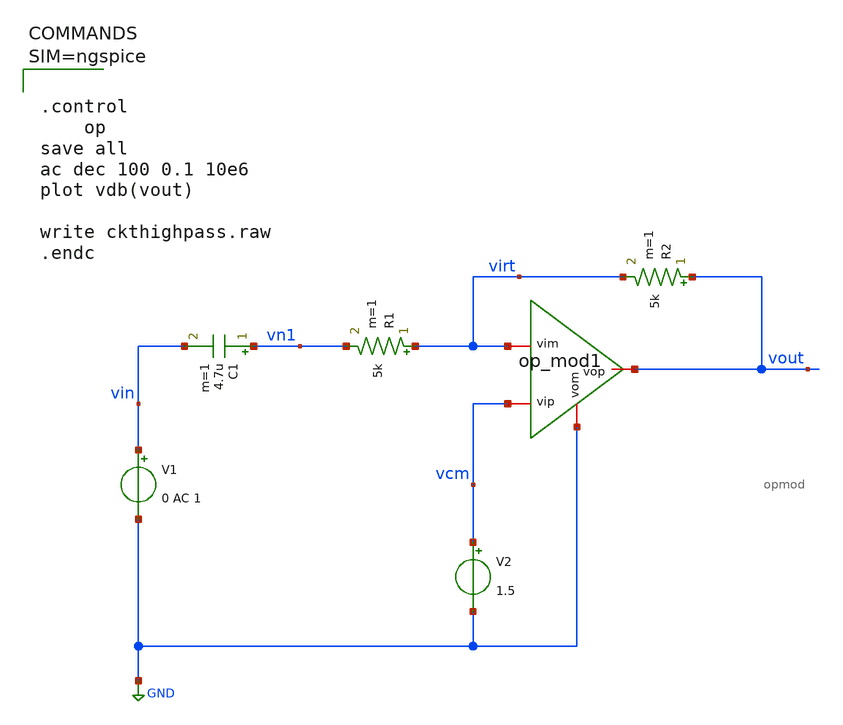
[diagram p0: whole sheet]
** sch_path: ckthighpass.sch
**.subckt ckthighpass
x1 vout vcm virt GND opmod
C1 vn1 vin 4.7u m=1
R1 virt vn1 5k m=1
V1 vin GND 0 AC 1
V2 vcm GND 1.5
R2 vout virt 5k m=1
**** begin user architecture code



.control
	op
save all
ac dec 100 0.1 10e6
plot vdb(vout)

write ckthighpass.raw
.endc



**** end user architecture code
**.ends

* expanding   symbol:  opmod.sym # of pins=4
** sym_path: opmod.sym
** sch_path: opmod.sch
.subckt opmod vop vip vim vom
*.iopin vop
*.iopin vom
*.iopin vim
*.iopin vip
E1 vop vom vip vim 1000
.ends

.GLOBAL GND
.end
